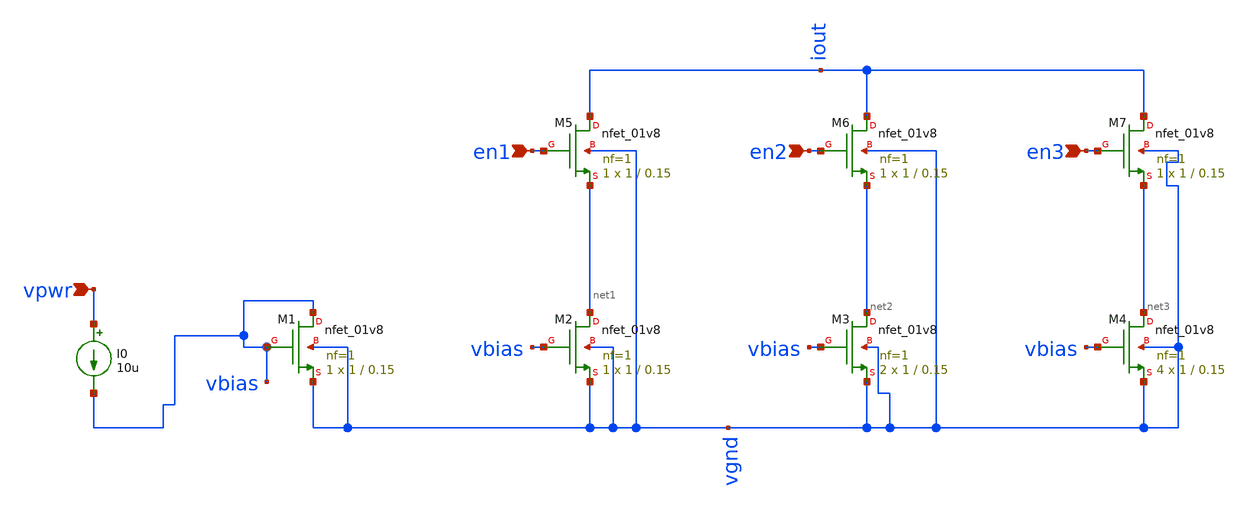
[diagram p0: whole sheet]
** sch_path: current_mirror.sch
**.subckt current_mirror vpwr en1 en2 en3
*.ipin vpwr
*.ipin en1
*.ipin en2
*.ipin en3
XM1 vbias vbias vgnd vgnd sky130_fd_pr__nfet_01v8 L=0.15 W=1 nf=1 ad='int((1 + 1)/2) * 1 / 1 * 0.29'
+ as='int((1 + 2)/2) * 1 / 1 * 0.29' pd='2*int((1 + 1)/2) * (1 / 1 + 0.29)' ps='2*int((1 + 2)/2) * (1 / 1 + 0.29)'
+ nrd='0.29 / 1 ' nrs='0.29 / 1 ' sa=0 sb=0 sd=0 mult=1 m=1
XM2 net1 vbias vgnd vgnd sky130_fd_pr__nfet_01v8 L=0.15 W=1 nf=1 ad='int((1 + 1)/2) * 1 / 1 * 0.29' as='int((1 + 2)/2) * 1 / 1 * 0.29'
+ pd='2*int((1 + 1)/2) * (1 / 1 + 0.29)' ps='2*int((1 + 2)/2) * (1 / 1 + 0.29)' nrd='0.29 / 1 ' nrs='0.29 / 1 '
+ sa=0 sb=0 sd=0 mult=1 m=1
XM3 net2 vbias vgnd vgnd sky130_fd_pr__nfet_01v8 L=0.15 W=1 nf=1 ad='int((1 + 1)/2) * 1 / 1 * 0.29' as='int((1 + 2)/2) * 1 / 1 * 0.29'
+ pd='2*int((1 + 1)/2) * (1 / 1 + 0.29)' ps='2*int((1 + 2)/2) * (1 / 1 + 0.29)' nrd='0.29 / 1 ' nrs='0.29 / 1 '
+ sa=0 sb=0 sd=0 mult=2 m=2
XM4 net3 vbias vgnd vgnd sky130_fd_pr__nfet_01v8 L=0.15 W=1 nf=1 ad='int((1 + 1)/2) * 1 / 1 * 0.29' as='int((1 + 2)/2) * 1 / 1 * 0.29'
+ pd='2*int((1 + 1)/2) * (1 / 1 + 0.29)' ps='2*int((1 + 2)/2) * (1 / 1 + 0.29)' nrd='0.29 / 1 ' nrs='0.29 / 1 '
+ sa=0 sb=0 sd=0 mult=4 m=4
XM5 iout en1 net1 vgnd sky130_fd_pr__nfet_01v8 L=0.15 W=1 nf=1 ad='int((1 + 1)/2) * 1 / 1 * 0.29' as='int((1 + 2)/2) * 1 / 1 * 0.29'
+ pd='2*int((1 + 1)/2) * (1 / 1 + 0.29)' ps='2*int((1 + 2)/2) * (1 / 1 + 0.29)' nrd='0.29 / 1 ' nrs='0.29 / 1 '
+ sa=0 sb=0 sd=0 mult=1 m=1
XM6 iout en2 net2 vgnd sky130_fd_pr__nfet_01v8 L=0.15 W=1 nf=1 ad='int((1 + 1)/2) * 1 / 1 * 0.29' as='int((1 + 2)/2) * 1 / 1 * 0.29'
+ pd='2*int((1 + 1)/2) * (1 / 1 + 0.29)' ps='2*int((1 + 2)/2) * (1 / 1 + 0.29)' nrd='0.29 / 1 ' nrs='0.29 / 1 '
+ sa=0 sb=0 sd=0 mult=1 m=1
XM7 iout en3 net3 vgnd sky130_fd_pr__nfet_01v8 L=0.15 W=1 nf=1 ad='int((1 + 1)/2) * 1 / 1 * 0.29' as='int((1 + 2)/2) * 1 / 1 * 0.29'
+ pd='2*int((1 + 1)/2) * (1 / 1 + 0.29)' ps='2*int((1 + 2)/2) * (1 / 1 + 0.29)' nrd='0.29 / 1 ' nrs='0.29 / 1 '
+ sa=0 sb=0 sd=0 mult=1 m=1
I0 vpwr vbias 10u
**** begin user architecture code


.lib /usr/local/share/pdk/sky130A/libs.tech/ngspice/sky130.lib.spice tt
.global vgnd
v_p vpwr vgnd 1.8
v_g vgnd 0 0
v_1 en1 vgnd 1.8
v_2 en2 vgnd 1.8
v_3 en3 vgnd 1.8
V1 iout vgnd 1.0

.control
dc V1 0.8 1.2 0.05
let curr_nominal = i(V1)

foreach run 1 2 3 4 5 6 7 8 9 10
  * Use loop index to generate a controlled spread around nominal
  let var_factor = 1.0 + (($run - 5.5) * 0.008)
  let curr_$run = curr_nominal * var_factor
end

plot curr_nominal curr_1 curr_2 curr_3 curr_4 curr_5 curr_6 curr_7 curr_8 curr_9 curr_10
.endc


**** end user architecture code
**.ends
.end
